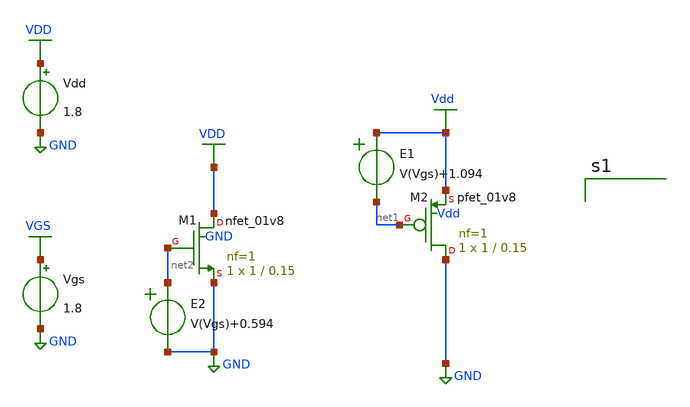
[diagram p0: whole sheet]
** sch_path: nmos-dc-corrected.sch
**.subckt nmos-dc-corrected
Vgs VGS GND 1.8
Vdd VDD GND 1.8
XM1 VDD net2 GND GND sky130_fd_pr__nfet_01v8 L=0.15 W=1 nf=1 ad='int((nf+1)/2) * W/nf * 0.29' as='int((nf+2)/2) * W/nf * 0.29'
+ pd='2*int((nf+1)/2) * (W/nf + 0.29)' ps='2*int((nf+2)/2) * (W/nf + 0.29)' nrd='0.29 / W' nrs='0.29 / W'
+ sa=0 sb=0 sd=0 mult=1 m=1
XM2 GND net1 Vdd Vdd sky130_fd_pr__pfet_01v8 L=0.15 W=1 nf=1 ad='int((nf+1)/2) * W/nf * 0.29' as='int((nf+2)/2) * W/nf * 0.29'
+ pd='2*int((nf+1)/2) * (W/nf + 0.29)' ps='2*int((nf+2)/2) * (W/nf + 0.29)' nrd='0.29 / W' nrs='0.29 / W'
+ sa=0 sb=0 sd=0 mult=1 m=1
E1 Vdd net1 VOL=' V(Vgs)+1.094 '
E2 net2 GND VOL=' V(Vgs)+0.594 '
**** begin user architecture code







**** end user architecture code
**.ends
.GLOBAL GND
.GLOBAL VGS
.GLOBAL VDD
.GLOBAL Vdd
.end
